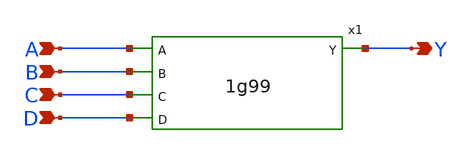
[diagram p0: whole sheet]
** sch_path: 1g99_test.sch
**.subckt 1g99_test A B C D Y
*.ipin A
*.ipin B
*.ipin C
*.ipin D
*.opin Y
x1 A B Y C D 1g99
**** begin user architecture code



VP VDD 0 dc 1.8
VA A 0 pulse(1.8 0 0 40p 40p 10n 20n) dc 0
VB B 0 pulse(1.8 0 0 40p 40p 20n 40n) dc 0
VC C 0 pulse(1.8 0 0 40p 40p 40n 80n) dc 0
VD D 0 pulse(1.8 0 0 40p 40p 80n 160n) dc 0
.control
save all
tran 10p 160n
meas tran test1 FIND v(y) WHEN time=5n > NUL
meas tran test2 FIND v(y) WHEN time=15n > NUL
meas tran test3 FIND v(y) WHEN time=25n > NUL
meas tran test4 FIND v(y) WHEN time=35n > NUL
meas tran test5 FIND v(y) WHEN time=45n > NUL
meas tran test6 FIND v(y) WHEN time=55n > NUL
meas tran test7 FIND v(y) WHEN time=65n > NUL
meas tran test8 FIND v(y) WHEN time=75n > NUL
meas tran test9 FIND v(y) WHEN time=85n > NUL
meas tran testa FIND v(y) WHEN time=95n > NUL
meas tran testb FIND v(y) WHEN time=105n > NUL
meas tran testc FIND v(y) WHEN time=115n > NUL
meas tran testd FIND v(y) WHEN time=125n > NUL
meas tran teste FIND v(y) WHEN time=135n > NUL
meas tran testf FIND v(y) WHEN time=145n > NUL
meas tran testg FIND v(y) WHEN time=155n > NUL
echo '*** TEST ***'
echo '-D-C-B-A-Y-'
echo -n '-L-L-L-L-'
if test1 >= 0.9
  echo 'H-'
else
  echo 'L-'
end
echo -n '-L-L-L-H-'
if test2 >= 0.9
  echo 'H-'
else
  echo 'L-'
end
echo -n '-L-L-H-L-'
if test3 >= 0.9
  echo 'H-'
else
  echo 'L-'
end
echo -n '-L-L-H-H-'
if test4 >= 0.9
  echo 'H-'
else
  echo 'L-'
end
echo -n '-L-H-L-L-'
if test5 >= 0.9
  echo 'H-'
else
  echo 'L-'
end
echo -n '-L-H-L-H-'
if test6 >= 0.9
  echo 'H-'
else
  echo 'L-'
end
echo -n '-L-H-H-L-'
if test7 >= 0.9
  echo 'H-'
else
  echo 'L-'
end
echo -n '-L-H-H-H-'
if test8 >= 0.9
  echo 'H-'
else
  echo 'L-'
end
echo -n '-H-L-L-L-'
if test9 >= 0.9
  echo 'H-'
else
  echo 'L-'
end
echo -n '-H-L-L-H-'
if testa >= 0.9
  echo 'H-'
else
  echo 'L-'
end
echo -n '-H-L-H-L-'
if testb >= 0.9
  echo 'H-'
else
  echo 'L-'
end
echo -n '-H-L-H-H-'
if testc >= 0.9
  echo 'H-'
else
  echo 'L-'
end
echo -n '-H-H-L-L-'
if testd >= 0.9
  echo 'H-'
else
  echo 'L-'
end
echo -n '-H-H-L-H-'
if teste >= 0.9
  echo 'H-'
else
  echo 'L-'
end
echo -n '-H-H-H-L-'
if testf >= 0.9
  echo 'H-'
else
  echo 'L-'
end
echo -n '-H-H-H-H-'
if testg >= 0.9
  echo 'H-'
else
  echo 'L-'
end
.endc



 .param mc_mm_switch=0
.param mc_pr_switch=0
.include $::SKYWATER_MODELS/corners/tt.spice
.include $::SKYWATER_MODELS/r+c/res_typical__cap_typical.spice
.include $::SKYWATER_MODELS/r+c/res_typical__cap_typical__lin.spice
.include $::SKYWATER_MODELS/corners/tt/specialized_cells.spice
.include $::SKYWATER_STDCELLS/sky130_fd_sc_hd.spice

**** end user architecture code
**.ends

* expanding   symbol:  1g99.sym # of pins=5
** sym_path: 1g99.sym
** sch_path: 1g99.sch
.subckt 1g99 A B Y C D
*.ipin A
*.ipin B
*.ipin C
*.ipin D
*.opin Y
.ends

.GLOBAL VDD
.GLOBAL GND
.end
